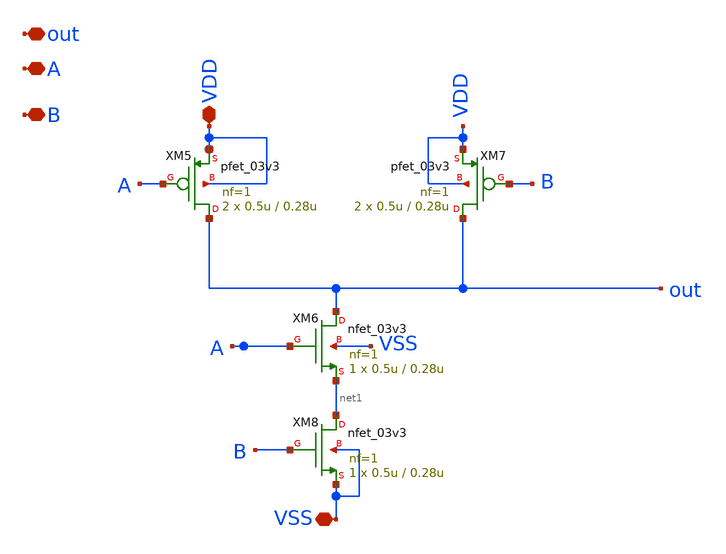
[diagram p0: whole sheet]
** sch_path: designs/sar_adc/digital/gate_nand_x1/xschem/gate_nand_x1.sch
**.subckt gate_nand_x1 A B out VDD VSS
*.iopin A
*.iopin B
*.iopin out
*.iopin VDD
*.iopin VSS
XM5 out A VDD VDD pfet_03v3 L=0.28u W=0.5u nf=1 ad='int((nf+1)/2) * W/nf * 0.18u' as='int((nf+2)/2) * W/nf * 0.18u'
+ pd='2*int((nf+1)/2) * (W/nf + 0.18u)' ps='2*int((nf+2)/2) * (W/nf + 0.18u)' nrd='0.18u / W' nrs='0.18u / W'
+ sa=0 sb=0 sd=0 m=2
XM6 out A net1 VSS nfet_03v3 L=0.28u W=0.5u nf=1 ad='int((nf+1)/2) * W/nf * 0.18u' as='int((nf+2)/2) * W/nf * 0.18u'
+ pd='2*int((nf+1)/2) * (W/nf + 0.18u)' ps='2*int((nf+2)/2) * (W/nf + 0.18u)' nrd='0.18u / W' nrs='0.18u / W'
+ sa=0 sb=0 sd=0 m=1
XM7 out B VDD VDD pfet_03v3 L=0.28u W=0.5u nf=1 ad='int((nf+1)/2) * W/nf * 0.18u' as='int((nf+2)/2) * W/nf * 0.18u'
+ pd='2*int((nf+1)/2) * (W/nf + 0.18u)' ps='2*int((nf+2)/2) * (W/nf + 0.18u)' nrd='0.18u / W' nrs='0.18u / W'
+ sa=0 sb=0 sd=0 m=2
XM8 net1 B VSS VSS nfet_03v3 L=0.28u W=0.5u nf=1 ad='int((nf+1)/2) * W/nf * 0.18u' as='int((nf+2)/2) * W/nf * 0.18u'
+ pd='2*int((nf+1)/2) * (W/nf + 0.18u)' ps='2*int((nf+2)/2) * (W/nf + 0.18u)' nrd='0.18u / W' nrs='0.18u / W'
+ sa=0 sb=0 sd=0 m=1
**.ends
.end
